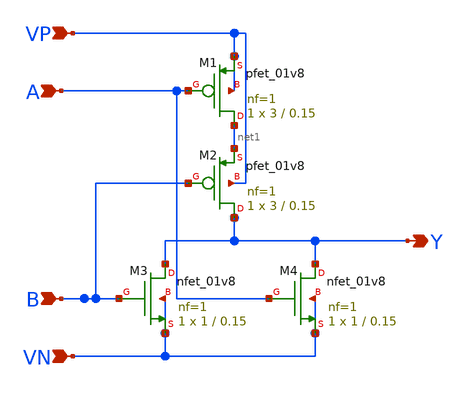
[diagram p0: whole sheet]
** sch_path: APIC-UTS/schematic/goldwin_nor/goldwin_nor.sch
**.subckt goldwin_nor A B VP VN Y
*.ipin A
*.ipin B
*.ipin VP
*.ipin VN
*.opin Y
XM1 net1 A VP VP sky130_fd_pr__pfet_01v8 L=0.15 W=3 nf=1 ad='int((nf+1)/2) * W/nf * 0.29' as='int((nf+2)/2) * W/nf * 0.29'
+ pd='2*int((nf+1)/2) * (W/nf + 0.29)' ps='2*int((nf+2)/2) * (W/nf + 0.29)' nrd='0.29 / W' nrs='0.29 / W'
+ sa=0 sb=0 sd=0 mult=1 m=1
XM2 Y B net1 VP sky130_fd_pr__pfet_01v8 L=0.15 W=3 nf=1 ad='int((nf+1)/2) * W/nf * 0.29' as='int((nf+2)/2) * W/nf * 0.29'
+ pd='2*int((nf+1)/2) * (W/nf + 0.29)' ps='2*int((nf+2)/2) * (W/nf + 0.29)' nrd='0.29 / W' nrs='0.29 / W'
+ sa=0 sb=0 sd=0 mult=1 m=1
XM3 Y B VN VN sky130_fd_pr__nfet_01v8 L=0.15 W=1 nf=1 ad='int((nf+1)/2) * W/nf * 0.29' as='int((nf+2)/2) * W/nf * 0.29'
+ pd='2*int((nf+1)/2) * (W/nf + 0.29)' ps='2*int((nf+2)/2) * (W/nf + 0.29)' nrd='0.29 / W' nrs='0.29 / W'
+ sa=0 sb=0 sd=0 mult=1 m=1
XM4 Y A VN VN sky130_fd_pr__nfet_01v8 L=0.15 W=1 nf=1 ad='int((nf+1)/2) * W/nf * 0.29' as='int((nf+2)/2) * W/nf * 0.29'
+ pd='2*int((nf+1)/2) * (W/nf + 0.29)' ps='2*int((nf+2)/2) * (W/nf + 0.29)' nrd='0.29 / W' nrs='0.29 / W'
+ sa=0 sb=0 sd=0 mult=1 m=1
**.ends
.end
